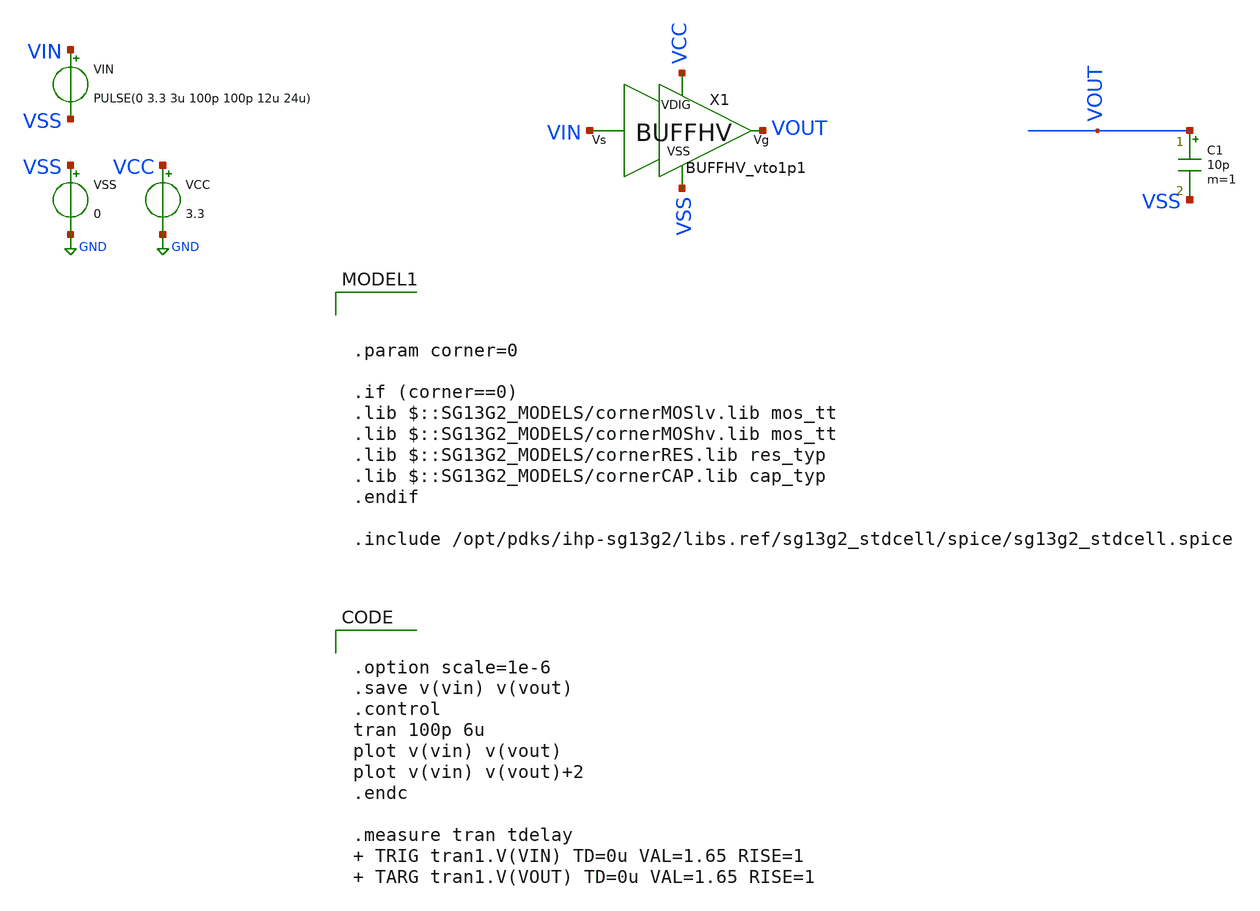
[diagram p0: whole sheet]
** sch_path: AC3E_USM_TDBUCK/design_data/xschem/BUFFHV/tb_BUFFHV_vto1p1.sch
**.subckt tb_BUFFHV_vto1p1
VCC VCC GND 3.3
VSS VSS GND 0
VIN VIN VSS PULSE(0 3.3 3u 100p 100p 12u 24u)
C1 VOUT VSS 10p m=1
X1 VIN VOUT VCC VSS BUFFHV_vto1p1
**** begin user architecture code


.option scale=1e-6
.save v(vin) v(vout)
.control
tran 100p 6u
plot v(vin) v(vout)
plot v(vin) v(vout)+2
.endc

.measure tran tdelay  TRIG tran1.V(VIN) TD=0u VAL=1.65 RISE=1  TARG tran1.V(VOUT) TD=0u VAL=1.65
+ RISE=1






.param corner=0

.if (corner==0)
.lib $::SG13G2_MODELS/cornerMOSlv.lib mos_tt
.lib $::SG13G2_MODELS/cornerMOShv.lib mos_tt
.lib $::SG13G2_MODELS/cornerRES.lib res_typ
.lib $::SG13G2_MODELS/cornerCAP.lib cap_typ
.endif

.include /opt/pdks/ihp-sg13g2/libs.ref/sg13g2_stdcell/spice/sg13g2_stdcell.spice

**** end user architecture code
**.ends
.GLOBAL GND
.end
